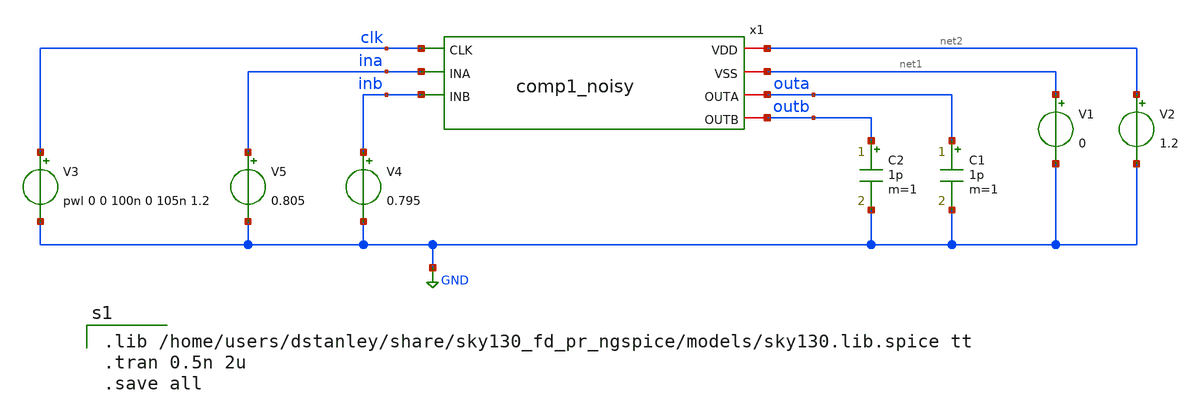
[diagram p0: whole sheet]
** sch_path: comp1_noisy_test.sch
**.subckt comp1_noisy_test
V1 net1 GND 0
V2 net2 GND 1.2
C1 outa GND 1p m=1
C2 outb GND 1p m=1
V3 clk GND pwl 0 0 100n 0 105n 1.2
V4 inb GND 0.795
V5 ina GND 0.805
x1 net2 net1 clk ina inb outa outb comp1_noisy
**** begin user architecture code

.lib /home/users/dstanley/share/sky130_fd_pr_ngspice/models/sky130.lib.spice tt
.tran 0.5n 2u
.save all

**** end user architecture code
**.ends

* expanding   symbol:  /home/users/dstanley/EE272B/xschem_tests/comp1_noisy.sym # of pins=7
** sym_path: comp1_noisy.sym
** sch_path: comp1_noisy.sch
.subckt comp1_noisy VDD VSS CLK INA INB OUTA OUTB
*.iopin VSS
*.iopin VDD
*.iopin OUTB
*.iopin OUTA
*.ipin INB
*.ipin INA
*.ipin CLK
XM1 net2 CLK VSS VSS sky130_fd_pr__nfet_01v8 L=0.15 W=1 nf=1 ad='int((nf+1)/2) * W/nf * 0.29' as='int((nf+2)/2) * W/nf * 0.29'
+ pd='2*int((nf+1)/2) * (W/nf + 0.29)' ps='2*int((nf+2)/2) * (W/nf + 0.29)' nrd='0.29 / W' nrs='0.29 / W'
+ sa=0 sb=0 sd=0 mult=1 m=1
XM2 net1 INA net2 VSS sky130_fd_pr__nfet_01v8 L=0.15 W=1 nf=1 ad='int((nf+1)/2) * W/nf * 0.29' as='int((nf+2)/2) * W/nf * 0.29'
+ pd='2*int((nf+1)/2) * (W/nf + 0.29)' ps='2*int((nf+2)/2) * (W/nf + 0.29)' nrd='0.29 / W' nrs='0.29 / W'
+ sa=0 sb=0 sd=0 mult=1 m=1
XM5 OUTB OUTA VDD VDD sky130_fd_pr__pfet_01v8 L=0.15 W=1 nf=1 ad='int((nf+1)/2) * W/nf * 0.29' as='int((nf+2)/2) * W/nf * 0.29'
+ pd='2*int((nf+1)/2) * (W/nf + 0.29)' ps='2*int((nf+2)/2) * (W/nf + 0.29)' nrd='0.29 / W' nrs='0.29 / W'
+ sa=0 sb=0 sd=0 mult=1 m=1
XM6 OUTB CLK VDD VDD sky130_fd_pr__pfet_01v8 L=0.15 W=1 nf=1 ad='int((nf+1)/2) * W/nf * 0.29' as='int((nf+2)/2) * W/nf * 0.29'
+ pd='2*int((nf+1)/2) * (W/nf + 0.29)' ps='2*int((nf+2)/2) * (W/nf + 0.29)' nrd='0.29 / W' nrs='0.29 / W'
+ sa=0 sb=0 sd=0 mult=1 m=1
XM3 net3 INB net2 VSS sky130_fd_pr__nfet_01v8 L=0.15 W=1 nf=1 ad='int((nf+1)/2) * W/nf * 0.29' as='int((nf+2)/2) * W/nf * 0.29'
+ pd='2*int((nf+1)/2) * (W/nf + 0.29)' ps='2*int((nf+2)/2) * (W/nf + 0.29)' nrd='0.29 / W' nrs='0.29 / W'
+ sa=0 sb=0 sd=0 mult=1 m=1
XM8 OUTA OUTB VDD VDD sky130_fd_pr__pfet_01v8 L=0.15 W=1 nf=1 ad='int((nf+1)/2) * W/nf * 0.29' as='int((nf+2)/2) * W/nf * 0.29'
+ pd='2*int((nf+1)/2) * (W/nf + 0.29)' ps='2*int((nf+2)/2) * (W/nf + 0.29)' nrd='0.29 / W' nrs='0.29 / W'
+ sa=0 sb=0 sd=0 mult=1 m=1
XM9 OUTA CLK VDD VDD sky130_fd_pr__pfet_01v8 L=0.15 W=1 nf=1 ad='int((nf+1)/2) * W/nf * 0.29' as='int((nf+2)/2) * W/nf * 0.29'
+ pd='2*int((nf+1)/2) * (W/nf + 0.29)' ps='2*int((nf+2)/2) * (W/nf + 0.29)' nrd='0.29 / W' nrs='0.29 / W'
+ sa=0 sb=0 sd=0 mult=1 m=1
x1 VSS OUTB OUTA net1 nmos_noisy
x2 VSS OUTA OUTB net3 nmos_noisy
.ends


* expanding   symbol:  /home/users/dstanley/EE272B/xschem_tests/nmos_noisy.sym # of pins=4
** sym_path: nmos_noisy.sym
** sch_path: nmos_noisy.sch
.subckt nmos_noisy B D G S
*.iopin S
*.ipin G
*.iopin D
*.ipin B
XM1 net1 G S B sky130_fd_pr__nfet_01v8 L=0.15 W=1 nf=1 ad='int((nf+1)/2) * W/nf * 0.29' as='int((nf+2)/2) * W/nf * 0.29'
+ pd='2*int((nf+1)/2) * (W/nf + 0.29)' ps='2*int((nf+2)/2) * (W/nf + 0.29)' nrd='0.29 / W' nrs='0.29 / W'
+ sa=0 sb=0 sd=0 mult=1 m=1
V1 noise_node S DC 0 trnoise(0 {noise_timestep} {oneoverf_exponent} {oneoverf_rms})
**** begin user architecture code

.param noise_max_freq=100MEG
.param noise_timestep={1/noise_max_freq}
.param oneoverf_exponent=0.8
.param oneoverf_rms=6.63n
.param i_nominal=14.46u

**** end user architecture code
B1 D S I = i(V2)/{i_nominal}*v(noise_node, S)
V2 D net1 dc 0
R1 noise_node S 1k m=1
.ends

.GLOBAL GND
.end
